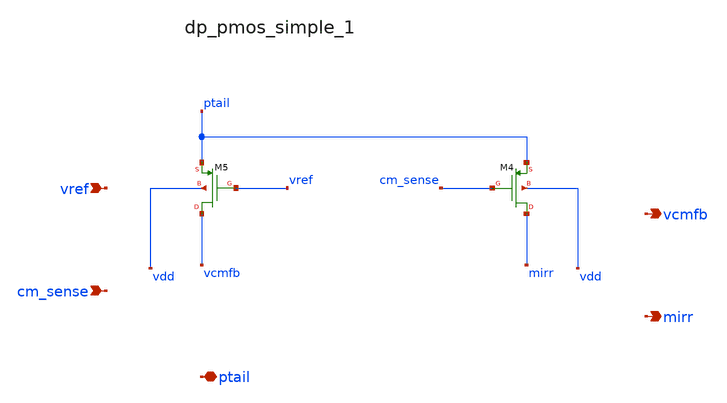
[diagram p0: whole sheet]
** sch_path: analog-db/raw/cmfb_002_5t_pmos_input/hier/blocks/dp_pmos_simple_1.sch
**.subckt dp_pmos_simple_1 vref cm_sense ptail vcmfb mirr
*.ipin vref
*.ipin cm_sense
*.iopin ptail
*.opin vcmfb
*.opin mirr
XM4 mirr cm_sense ptail vdd sg13_lv_pmos w=x_dut_xm4_w l=x_dut_xm4_l ng=1 m=x_dut_xm4_m
XM5 vcmfb vref ptail vdd sg13_lv_pmos w=x_dut_xm5_w l=x_dut_xm5_l ng=1 m=x_dut_xm5_m
**.ends
.end
